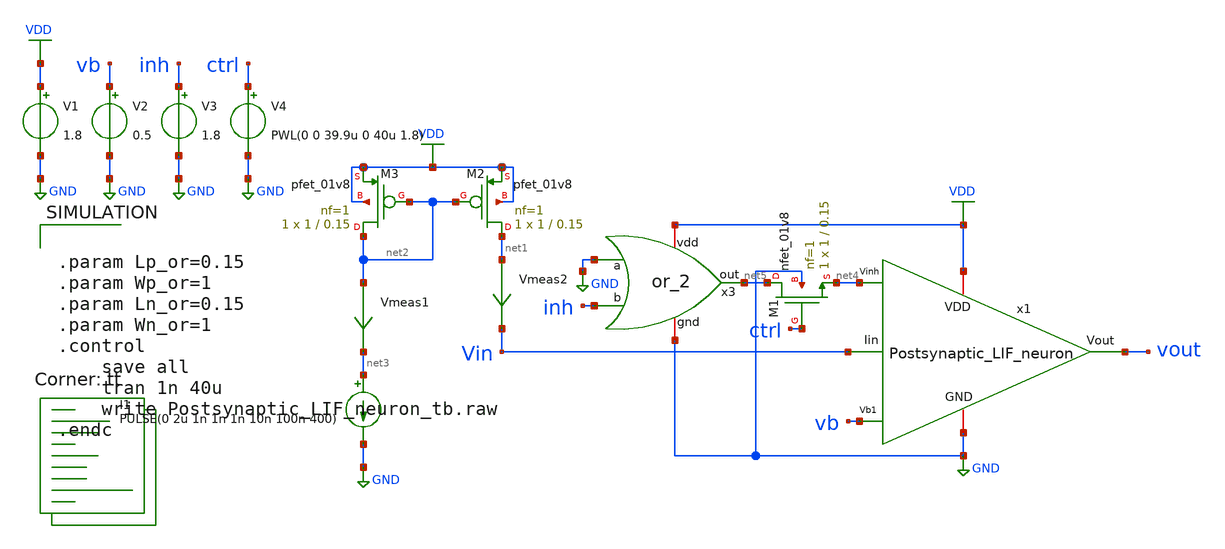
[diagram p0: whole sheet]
** sch_path: LIF_neuron/Postsynaptic_LIF_neuron_tb.sch
**.subckt Postsynaptic_LIF_neuron_tb
V1 VDD GND 1.8
V2 vb GND 0.5
x1 Vin VDD vout vb GND net4 Postsynaptic_LIF_neuron
I1 net3 GND PULSE(0 2u 1n 1n 1n 10n 100n 400)
XM2 net1 net2 VDD VDD sky130_fd_pr__pfet_01v8 L=0.15 W=1 nf=1 ad='int((nf+1)/2) * W/nf * 0.29' as='int((nf+2)/2) * W/nf * 0.29'
+ pd='2*int((nf+1)/2) * (W/nf + 0.29)' ps='2*int((nf+2)/2) * (W/nf + 0.29)' nrd='0.29 / W' nrs='0.29 / W'
+ sa=0 sb=0 sd=0 mult=1 m=1
XM3 net2 net2 VDD VDD sky130_fd_pr__pfet_01v8 L=0.15 W=1 nf=1 ad='int((nf+1)/2) * W/nf * 0.29' as='int((nf+2)/2) * W/nf * 0.29'
+ pd='2*int((nf+1)/2) * (W/nf + 0.29)' ps='2*int((nf+2)/2) * (W/nf + 0.29)' nrd='0.29 / W' nrs='0.29 / W'
+ sa=0 sb=0 sd=0 mult=1 m=1
Vmeas1 net2 net3 0
.save i(vmeas1)
Vmeas2 net1 Vin 0
.save i(vmeas2)
V4 ctrl GND PWL(0 0 39.9u 0 40u 1.8)
x3 VDD GND inh net5 GND or_2
XM1 net5 ctrl net4 GND sky130_fd_pr__nfet_01v8 L=0.15 W=1 nf=1 ad='int((nf+1)/2) * W/nf * 0.29' as='int((nf+2)/2) * W/nf * 0.29'
+ pd='2*int((nf+1)/2) * (W/nf + 0.29)' ps='2*int((nf+2)/2) * (W/nf + 0.29)' nrd='0.29 / W' nrs='0.29 / W'
+ sa=0 sb=0 sd=0 mult=1 m=1
V3 inh GND 1.8
**** begin user architecture code


.param Lp_or=0.15
.param Wp_or=1
.param Ln_or=0.15
.param Wn_or=1
.control
	save all
	tran 1n 40u
	write Postsynaptic_LIF_neuron_tb.raw
.endc


.lib $::SKYWATER_MODELS/sky130.lib.spice tt
**** end user architecture code
**.ends

* expanding   symbol:
*+  /home/ricardo/RATT_repos/Proyectos_xschem/LIF_neuron/Postsynaptic_LIF_neuron.sym # of pins=6
** sym_path: LIF_neuron/Postsynaptic_LIF_neuron.sym
** sch_path: LIF_neuron/Postsynaptic_LIF_neuron.sch
.subckt Postsynaptic_LIF_neuron Iin VDD Vout Vb1 GND Vinh
*.iopin GND
*.ipin Vb1
*.iopin VDD
*.opin Vout
*.ipin Iin
*.ipin Vinh
XM13 net2 Vb1 GND GND sky130_fd_pr__nfet_01v8 L=0.5 W=5 nf=1 ad='int((nf+1)/2) * W/nf * 0.29' as='int((nf+2)/2) * W/nf * 0.29'
+ pd='2*int((nf+1)/2) * (W/nf + 0.29)' ps='2*int((nf+2)/2) * (W/nf + 0.29)' nrd='0.29 / W' nrs='0.29 / W'
+ sa=0 sb=0 sd=0 mult=1 m=1
XM12 Vinh net1 net2 GND sky130_fd_pr__nfet_01v8 L=1 W=1 nf=1 ad='int((nf+1)/2) * W/nf * 0.29' as='int((nf+2)/2) * W/nf * 0.29'
+ pd='2*int((nf+1)/2) * (W/nf + 0.29)' ps='2*int((nf+2)/2) * (W/nf + 0.29)' nrd='0.29 / W' nrs='0.29 / W'
+ sa=0 sb=0 sd=0 mult=1 m=1
XM11 Vinh net1 VDD VDD sky130_fd_pr__pfet_01v8 L=1 W=1 nf=1 ad='int((nf+1)/2) * W/nf * 0.29' as='int((nf+2)/2) * W/nf * 0.29'
+ pd='2*int((nf+1)/2) * (W/nf + 0.29)' ps='2*int((nf+2)/2) * (W/nf + 0.29)' nrd='0.29 / W' nrs='0.29 / W'
+ sa=0 sb=0 sd=0 mult=1 m=1
XC1 Vinh GND sky130_fd_pr__cap_mim_m3_1 W=11 L=1 MF=1 m=1
XM14 Iin Vinh GND GND sky130_fd_pr__nfet_01v8 L=5 W=1 nf=1 ad='int((nf+1)/2) * W/nf * 0.29' as='int((nf+2)/2) * W/nf * 0.29'
+ pd='2*int((nf+1)/2) * (W/nf + 0.29)' ps='2*int((nf+2)/2) * (W/nf + 0.29)' nrd='0.29 / W' nrs='0.29 / W'
+ sa=0 sb=0 sd=0 mult=1 m=1
XC2 Iin GND sky130_fd_pr__cap_mim_m3_1 W=10 L=10 MF=10 m=10
XM6 net3 Vout GND GND sky130_fd_pr__nfet_01v8 L=0.5 W=1 nf=1 ad='int((nf+1)/2) * W/nf * 0.29' as='int((nf+2)/2) * W/nf * 0.29'
+ pd='2*int((nf+1)/2) * (W/nf + 0.29)' ps='2*int((nf+2)/2) * (W/nf + 0.29)' nrd='0.29 / W' nrs='0.29 / W'
+ sa=0 sb=0 sd=0 mult=1 m=1
XM7 net1 Iin net3 GND sky130_fd_pr__nfet_01v8 L=1 W=1 nf=1 ad='int((nf+1)/2) * W/nf * 0.29' as='int((nf+2)/2) * W/nf * 0.29'
+ pd='2*int((nf+1)/2) * (W/nf + 0.29)' ps='2*int((nf+2)/2) * (W/nf + 0.29)' nrd='0.29 / W' nrs='0.29 / W'
+ sa=0 sb=0 sd=0 mult=1 m=1
XM8 net1 Iin VDD VDD sky130_fd_pr__pfet_01v8 L=1 W=1 nf=1 ad='int((nf+1)/2) * W/nf * 0.29' as='int((nf+2)/2) * W/nf * 0.29'
+ pd='2*int((nf+1)/2) * (W/nf + 0.29)' ps='2*int((nf+2)/2) * (W/nf + 0.29)' nrd='0.29 / W' nrs='0.29 / W'
+ sa=0 sb=0 sd=0 mult=1 m=1
XM9 Vout net1 net3 GND sky130_fd_pr__nfet_01v8 L=1 W=1 nf=1 ad='int((nf+1)/2) * W/nf * 0.29' as='int((nf+2)/2) * W/nf * 0.29'
+ pd='2*int((nf+1)/2) * (W/nf + 0.29)' ps='2*int((nf+2)/2) * (W/nf + 0.29)' nrd='0.29 / W' nrs='0.29 / W'
+ sa=0 sb=0 sd=0 mult=1 m=1
XM10 Vout net1 VDD VDD sky130_fd_pr__pfet_01v8 L=1 W=5 nf=1 ad='int((nf+1)/2) * W/nf * 0.29' as='int((nf+2)/2) * W/nf * 0.29'
+ pd='2*int((nf+1)/2) * (W/nf + 0.29)' ps='2*int((nf+2)/2) * (W/nf + 0.29)' nrd='0.29 / W' nrs='0.29 / W'
+ sa=0 sb=0 sd=0 mult=1 m=1
.ends


* expanding   symbol:  /home/ricardo/RATT_repos/Proyectos_xschem/inhibitory/or_2.sym # of pins=5
** sym_path: inhibitory/or_2.sym
** sch_path: inhibitory/or_2.sch
.subckt or_2 vdd a b out gnd
*.iopin gnd
*.ipin a
*.ipin b
*.opin out
*.iopin vdd
XM1 net1 a vdd vdd sky130_fd_pr__pfet_01v8 L={Lp_or} W={Wp_or} nf=1 ad='int((nf+1)/2) * W/nf * 0.29'
+ as='int((nf+2)/2) * W/nf * 0.29' pd='2*int((nf+1)/2) * (W/nf + 0.29)' ps='2*int((nf+2)/2) * (W/nf + 0.29)'
+ nrd='0.29 / W' nrs='0.29 / W' sa=0 sb=0 sd=0 mult=1 m=1
XM2 net2 b gnd gnd sky130_fd_pr__nfet_01v8 L={Ln_or} W={Wn_or} nf=1 ad='int((nf+1)/2) * W/nf * 0.29'
+ as='int((nf+2)/2) * W/nf * 0.29' pd='2*int((nf+1)/2) * (W/nf + 0.29)' ps='2*int((nf+2)/2) * (W/nf + 0.29)'
+ nrd='0.29 / W' nrs='0.29 / W' sa=0 sb=0 sd=0 mult=1 m=1
XM3 net2 b net1 vdd sky130_fd_pr__pfet_01v8 L={Lp_or} W={Wp_or} nf=1 ad='int((nf+1)/2) * W/nf * 0.29'
+ as='int((nf+2)/2) * W/nf * 0.29' pd='2*int((nf+1)/2) * (W/nf + 0.29)' ps='2*int((nf+2)/2) * (W/nf + 0.29)'
+ nrd='0.29 / W' nrs='0.29 / W' sa=0 sb=0 sd=0 mult=1 m=1
XM4 net2 a gnd gnd sky130_fd_pr__nfet_01v8 L={Ln_or} W={Wn_or} nf=1 ad='int((nf+1)/2) * W/nf * 0.29'
+ as='int((nf+2)/2) * W/nf * 0.29' pd='2*int((nf+1)/2) * (W/nf + 0.29)' ps='2*int((nf+2)/2) * (W/nf + 0.29)'
+ nrd='0.29 / W' nrs='0.29 / W' sa=0 sb=0 sd=0 mult=1 m=1
XM5 out net2 gnd gnd sky130_fd_pr__nfet_01v8 L={Ln_or} W={Wn_or} nf=1 ad='int((nf+1)/2) * W/nf * 0.29'
+ as='int((nf+2)/2) * W/nf * 0.29' pd='2*int((nf+1)/2) * (W/nf + 0.29)' ps='2*int((nf+2)/2) * (W/nf + 0.29)'
+ nrd='0.29 / W' nrs='0.29 / W' sa=0 sb=0 sd=0 mult=1 m=1
XM6 out net2 vdd vdd sky130_fd_pr__pfet_01v8 L={Lp_or} W={Wp_or} nf=1 ad='int((nf+1)/2) * W/nf * 0.29'
+ as='int((nf+2)/2) * W/nf * 0.29' pd='2*int((nf+1)/2) * (W/nf + 0.29)' ps='2*int((nf+2)/2) * (W/nf + 0.29)'
+ nrd='0.29 / W' nrs='0.29 / W' sa=0 sb=0 sd=0 mult=1 m=1
.ends

.GLOBAL GND
.GLOBAL VDD
.end
